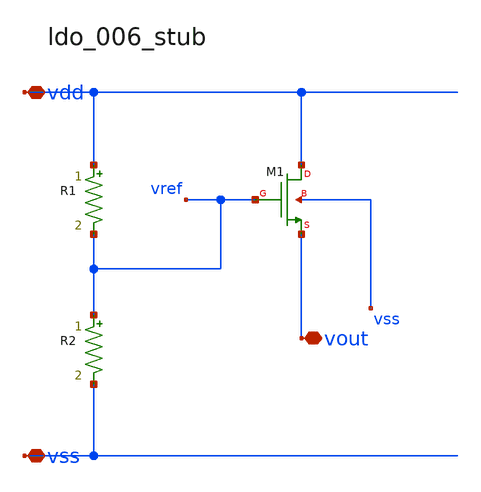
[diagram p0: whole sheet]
** sch_path: analog-db/raw/ldo_006_stub/ldo_006_stub_annotated.sch
**.subckt ldo_006_stub_annotated vdd vout vss
*.iopin vdd
*.iopin vout
*.iopin vss
R1 vdd vref r_top m=1
R2 vref vss r_bot m=1
XM1 vdd vref vout vss sg13_lv_nmos w=x_dut_xm1_w l=x_dut_xm1_l ng=1 m=x_dut_xm1_m
**.ends
.end
